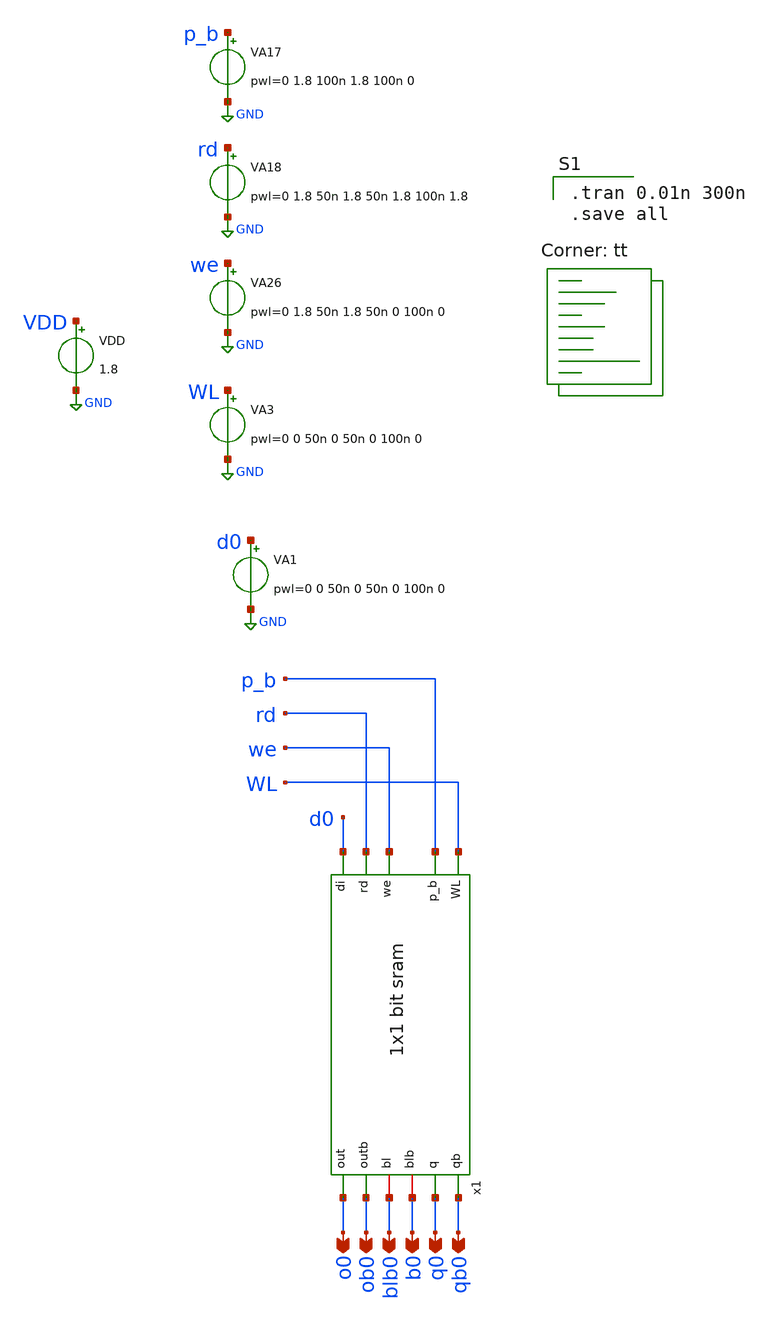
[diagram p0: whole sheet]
** sch_path: gates/Memory/1 bit sram sym sim.sch
**.subckt 1 bit sram sym sim o0 ob0 blb0 b0 q0 qb0
*.opin o0
*.opin ob0
*.opin blb0
*.opin b0
*.opin q0
*.opin qb0
x1 WL qb0 q0 b0 blb0 p_b we rd ob0 o0 d0 1x1 bit sram
VA17 p_b GND pwl=0 1.8 100n 1.8 100n 0
VA18 rd GND pwl=0 1.8 50n 1.8 50n 1.8 100n 1.8
VA26 we GND pwl=0 1.8 50n 1.8 50n 0 100n 0
VA3 WL GND pwl=0 0 50n 0 50n 0 100n 0
VDD VDD GND 1.8
VA1 d0 GND pwl=0 0 50n 0 50n 0 100n 0
**** begin user architecture code

.tran 0.01n 300n
.save all

.lib $::SKYWATER_MODELS/sky130.lib.spice tt
**** end user architecture code
**.ends

* expanding   symbol:  Memory/1x1 bit sram.sym # of pins=11
** sym_path: gates/Memory/1x1 bit sram.sym
** sch_path: gates/Memory/1x1 bit sram.sch
.subckt 1x1 bit sram WL qb q blb bl p_b we rd outb out di
*.ipin WL
*.opin qb
*.opin q
*.ipin we
*.ipin di
*.ipin p_b
*.ipin rd
*.opin out
*.opin outb
*.iopin blb
*.iopin bl
XM1 qb q VDD VDD sky130_fd_pr__pfet_01v8 L=0.15 W=1 nf=1 ad='int((nf+1)/2) * W/nf * 0.29' as='int((nf+2)/2) * W/nf * 0.29'
+ pd='2*int((nf+1)/2) * (W/nf + 0.29)' ps='2*int((nf+2)/2) * (W/nf + 0.29)' nrd='0.29 / W' nrs='0.29 / W'
+ sa=0 sb=0 sd=0 mult=1 m=1
XM2 qb q GND GND sky130_fd_pr__nfet_01v8 L=0.15 W=1 nf=1 ad='int((nf+1)/2) * W/nf * 0.29' as='int((nf+2)/2) * W/nf * 0.29'
+ pd='2*int((nf+1)/2) * (W/nf + 0.29)' ps='2*int((nf+2)/2) * (W/nf + 0.29)' nrd='0.29 / W' nrs='0.29 / W'
+ sa=0 sb=0 sd=0 mult=1 m=1
XM3 q qb VDD VDD sky130_fd_pr__pfet_01v8 L=0.15 W=1 nf=1 ad='int((nf+1)/2) * W/nf * 0.29' as='int((nf+2)/2) * W/nf * 0.29'
+ pd='2*int((nf+1)/2) * (W/nf + 0.29)' ps='2*int((nf+2)/2) * (W/nf + 0.29)' nrd='0.29 / W' nrs='0.29 / W'
+ sa=0 sb=0 sd=0 mult=1 m=1
XM4 q qb GND GND sky130_fd_pr__nfet_01v8 L=0.15 W=1 nf=1 ad='int((nf+1)/2) * W/nf * 0.29' as='int((nf+2)/2) * W/nf * 0.29'
+ pd='2*int((nf+1)/2) * (W/nf + 0.29)' ps='2*int((nf+2)/2) * (W/nf + 0.29)' nrd='0.29 / W' nrs='0.29 / W'
+ sa=0 sb=0 sd=0 mult=1 m=1
XM5 bl WL q GND sky130_fd_pr__nfet_01v8 L=0.15 W=1 nf=1 ad='int((nf+1)/2) * W/nf * 0.29' as='int((nf+2)/2) * W/nf * 0.29'
+ pd='2*int((nf+1)/2) * (W/nf + 0.29)' ps='2*int((nf+2)/2) * (W/nf + 0.29)' nrd='0.29 / W' nrs='0.29 / W'
+ sa=0 sb=0 sd=0 mult=1 m=1
XM6 qb WL blb GND sky130_fd_pr__nfet_01v8 L=0.15 W=1 nf=1 ad='int((nf+1)/2) * W/nf * 0.29' as='int((nf+2)/2) * W/nf * 0.29'
+ pd='2*int((nf+1)/2) * (W/nf + 0.29)' ps='2*int((nf+2)/2) * (W/nf + 0.29)' nrd='0.29 / W' nrs='0.29 / W'
+ sa=0 sb=0 sd=0 mult=1 m=1
X1 we net7 inv_vtc
X5 di net3 inv_vtc
XM7 net5 net7 VDD VDD sky130_fd_pr__pfet_01v8 L=0.15 W=1 nf=1 ad='int((nf+1)/2) * W/nf * 0.29' as='int((nf+2)/2) * W/nf * 0.29'
+ pd='2*int((nf+1)/2) * (W/nf + 0.29)' ps='2*int((nf+2)/2) * (W/nf + 0.29)' nrd='0.29 / W' nrs='0.29 / W'
+ sa=0 sb=0 sd=0 mult=1 m=1
XM8 blb di net5 VDD sky130_fd_pr__pfet_01v8 L=0.15 W=1 nf=1 ad='int((nf+1)/2) * W/nf * 0.29' as='int((nf+2)/2) * W/nf * 0.29'
+ pd='2*int((nf+1)/2) * (W/nf + 0.29)' ps='2*int((nf+2)/2) * (W/nf + 0.29)' nrd='0.29 / W' nrs='0.29 / W'
+ sa=0 sb=0 sd=0 mult=1 m=1
XM9 blb di net6 GND sky130_fd_pr__nfet_01v8 L=0.15 W=1 nf=1 ad='int((nf+1)/2) * W/nf * 0.29' as='int((nf+2)/2) * W/nf * 0.29'
+ pd='2*int((nf+1)/2) * (W/nf + 0.29)' ps='2*int((nf+2)/2) * (W/nf + 0.29)' nrd='0.29 / W' nrs='0.29 / W'
+ sa=0 sb=0 sd=0 mult=1 m=1
XM10 net6 we GND GND sky130_fd_pr__nfet_01v8 L=0.15 W=1 nf=1 ad='int((nf+1)/2) * W/nf * 0.29' as='int((nf+2)/2) * W/nf * 0.29'
+ pd='2*int((nf+1)/2) * (W/nf + 0.29)' ps='2*int((nf+2)/2) * (W/nf + 0.29)' nrd='0.29 / W' nrs='0.29 / W'
+ sa=0 sb=0 sd=0 mult=1 m=1
XM11 net1 net7 VDD VDD sky130_fd_pr__pfet_01v8 L=0.15 W=1 nf=1 ad='int((nf+1)/2) * W/nf * 0.29' as='int((nf+2)/2) * W/nf * 0.29'
+ pd='2*int((nf+1)/2) * (W/nf + 0.29)' ps='2*int((nf+2)/2) * (W/nf + 0.29)' nrd='0.29 / W' nrs='0.29 / W'
+ sa=0 sb=0 sd=0 mult=1 m=1
XM12 bl net3 net1 VDD sky130_fd_pr__pfet_01v8 L=0.15 W=1 nf=1 ad='int((nf+1)/2) * W/nf * 0.29' as='int((nf+2)/2) * W/nf * 0.29'
+ pd='2*int((nf+1)/2) * (W/nf + 0.29)' ps='2*int((nf+2)/2) * (W/nf + 0.29)' nrd='0.29 / W' nrs='0.29 / W'
+ sa=0 sb=0 sd=0 mult=1 m=1
XM13 bl net3 net2 GND sky130_fd_pr__nfet_01v8 L=0.15 W=1 nf=1 ad='int((nf+1)/2) * W/nf * 0.29' as='int((nf+2)/2) * W/nf * 0.29'
+ pd='2*int((nf+1)/2) * (W/nf + 0.29)' ps='2*int((nf+2)/2) * (W/nf + 0.29)' nrd='0.29 / W' nrs='0.29 / W'
+ sa=0 sb=0 sd=0 mult=1 m=1
XM14 net2 we GND GND sky130_fd_pr__nfet_01v8 L=0.15 W=1 nf=1 ad='int((nf+1)/2) * W/nf * 0.29' as='int((nf+2)/2) * W/nf * 0.29'
+ pd='2*int((nf+1)/2) * (W/nf + 0.29)' ps='2*int((nf+2)/2) * (W/nf + 0.29)' nrd='0.29 / W' nrs='0.29 / W'
+ sa=0 sb=0 sd=0 mult=1 m=1
XM15 bl p_b VDD VDD sky130_fd_pr__pfet_01v8 L=0.15 W=1 nf=1 ad='int((nf+1)/2) * W/nf * 0.29' as='int((nf+2)/2) * W/nf * 0.29'
+ pd='2*int((nf+1)/2) * (W/nf + 0.29)' ps='2*int((nf+2)/2) * (W/nf + 0.29)' nrd='0.29 / W' nrs='0.29 / W'
+ sa=0 sb=0 sd=0 mult=1 m=1
XM16 blb p_b bl VDD sky130_fd_pr__pfet_01v8 L=0.15 W=1 nf=1 ad='int((nf+1)/2) * W/nf * 0.29' as='int((nf+2)/2) * W/nf * 0.29'
+ pd='2*int((nf+1)/2) * (W/nf + 0.29)' ps='2*int((nf+2)/2) * (W/nf + 0.29)' nrd='0.29 / W' nrs='0.29 / W'
+ sa=0 sb=0 sd=0 mult=1 m=1
XM17 blb p_b VDD VDD sky130_fd_pr__pfet_01v8 L=0.15 W=1 nf=1 ad='int((nf+1)/2) * W/nf * 0.29' as='int((nf+2)/2) * W/nf * 0.29'
+ pd='2*int((nf+1)/2) * (W/nf + 0.29)' ps='2*int((nf+2)/2) * (W/nf + 0.29)' nrd='0.29 / W' nrs='0.29 / W'
+ sa=0 sb=0 sd=0 mult=1 m=1
XM18 out p_b VDD VDD sky130_fd_pr__pfet_01v8 L=0.15 W=1 nf=1 ad='int((nf+1)/2) * W/nf * 0.29' as='int((nf+2)/2) * W/nf * 0.29'
+ pd='2*int((nf+1)/2) * (W/nf + 0.29)' ps='2*int((nf+2)/2) * (W/nf + 0.29)' nrd='0.29 / W' nrs='0.29 / W'
+ sa=0 sb=0 sd=0 mult=1 m=1
XM19 outb p_b out VDD sky130_fd_pr__pfet_01v8 L=0.15 W=1 nf=1 ad='int((nf+1)/2) * W/nf * 0.29' as='int((nf+2)/2) * W/nf * 0.29'
+ pd='2*int((nf+1)/2) * (W/nf + 0.29)' ps='2*int((nf+2)/2) * (W/nf + 0.29)' nrd='0.29 / W' nrs='0.29 / W'
+ sa=0 sb=0 sd=0 mult=1 m=1
XM20 outb p_b VDD VDD sky130_fd_pr__pfet_01v8 L=0.15 W=1 nf=1 ad='int((nf+1)/2) * W/nf * 0.29' as='int((nf+2)/2) * W/nf * 0.29'
+ pd='2*int((nf+1)/2) * (W/nf + 0.29)' ps='2*int((nf+2)/2) * (W/nf + 0.29)' nrd='0.29 / W' nrs='0.29 / W'
+ sa=0 sb=0 sd=0 mult=1 m=1
XM21 out outb VDD VDD sky130_fd_pr__pfet_01v8 L=0.15 W=1 nf=1 ad='int((nf+1)/2) * W/nf * 0.29' as='int((nf+2)/2) * W/nf * 0.29'
+ pd='2*int((nf+1)/2) * (W/nf + 0.29)' ps='2*int((nf+2)/2) * (W/nf + 0.29)' nrd='0.29 / W' nrs='0.29 / W'
+ sa=0 sb=0 sd=0 mult=1 m=1
XM22 outb out VDD VDD sky130_fd_pr__pfet_01v8 L=0.15 W=1 nf=1 ad='int((nf+1)/2) * W/nf * 0.29' as='int((nf+2)/2) * W/nf * 0.29'
+ pd='2*int((nf+1)/2) * (W/nf + 0.29)' ps='2*int((nf+2)/2) * (W/nf + 0.29)' nrd='0.29 / W' nrs='0.29 / W'
+ sa=0 sb=0 sd=0 mult=1 m=1
XM23 outb out net4 GND sky130_fd_pr__nfet_01v8 L=0.15 W=1 nf=1 ad='int((nf+1)/2) * W/nf * 0.29' as='int((nf+2)/2) * W/nf * 0.29'
+ pd='2*int((nf+1)/2) * (W/nf + 0.29)' ps='2*int((nf+2)/2) * (W/nf + 0.29)' nrd='0.29 / W' nrs='0.29 / W'
+ sa=0 sb=0 sd=0 mult=1 m=1
XM24 out outb net4 GND sky130_fd_pr__nfet_01v8 L=0.15 W=1 nf=1 ad='int((nf+1)/2) * W/nf * 0.29' as='int((nf+2)/2) * W/nf * 0.29'
+ pd='2*int((nf+1)/2) * (W/nf + 0.29)' ps='2*int((nf+2)/2) * (W/nf + 0.29)' nrd='0.29 / W' nrs='0.29 / W'
+ sa=0 sb=0 sd=0 mult=1 m=1
XM25 net4 VDD GND GND sky130_fd_pr__nfet_01v8 L=0.15 W=1 nf=1 ad='int((nf+1)/2) * W/nf * 0.29' as='int((nf+2)/2) * W/nf * 0.29'
+ pd='2*int((nf+1)/2) * (W/nf + 0.29)' ps='2*int((nf+2)/2) * (W/nf + 0.29)' nrd='0.29 / W' nrs='0.29 / W'
+ sa=0 sb=0 sd=0 mult=1 m=1
XM26 bl rd out VDD sky130_fd_pr__pfet_01v8 L=0.15 W=1 nf=1 ad='int((nf+1)/2) * W/nf * 0.29' as='int((nf+2)/2) * W/nf * 0.29'
+ pd='2*int((nf+1)/2) * (W/nf + 0.29)' ps='2*int((nf+2)/2) * (W/nf + 0.29)' nrd='0.29 / W' nrs='0.29 / W'
+ sa=0 sb=0 sd=0 mult=1 m=1
XM27 outb rd blb VDD sky130_fd_pr__pfet_01v8 L=0.15 W=1 nf=1 ad='int((nf+1)/2) * W/nf * 0.29' as='int((nf+2)/2) * W/nf * 0.29'
+ pd='2*int((nf+1)/2) * (W/nf + 0.29)' ps='2*int((nf+2)/2) * (W/nf + 0.29)' nrd='0.29 / W' nrs='0.29 / W'
+ sa=0 sb=0 sd=0 mult=1 m=1
.ends


* expanding   symbol:  /home/apn/test_xschem_sky130/inv_vtc.sym # of pins=2
** sym_path: gates/Memory/inv_vtc.sym
** sch_path: gates/Memory/inv_vtc.sch
.subckt inv_vtc A Y
*.ipin A
*.opin Y
XM1 Y A VDD VDD sky130_fd_pr__pfet_01v8 L=0.15 W=2 nf=1 ad='int((nf+1)/2) * W/nf * 0.29' as='int((nf+2)/2) * W/nf * 0.29'
+ pd='2*int((nf+1)/2) * (W/nf + 0.29)' ps='2*int((nf+2)/2) * (W/nf + 0.29)' nrd='0.29 / W' nrs='0.29 / W'
+ sa=0 sb=0 sd=0 mult=1 m=1
XM2 Y A GND GND sky130_fd_pr__nfet_01v8 L=0.15 W=1 nf=1 ad='int((nf+1)/2) * W/nf * 0.29' as='int((nf+2)/2) * W/nf * 0.29'
+ pd='2*int((nf+1)/2) * (W/nf + 0.29)' ps='2*int((nf+2)/2) * (W/nf + 0.29)' nrd='0.29 / W' nrs='0.29 / W'
+ sa=0 sb=0 sd=0 mult=1 m=1
.ends

.GLOBAL GND
.GLOBAL VDD
.end
